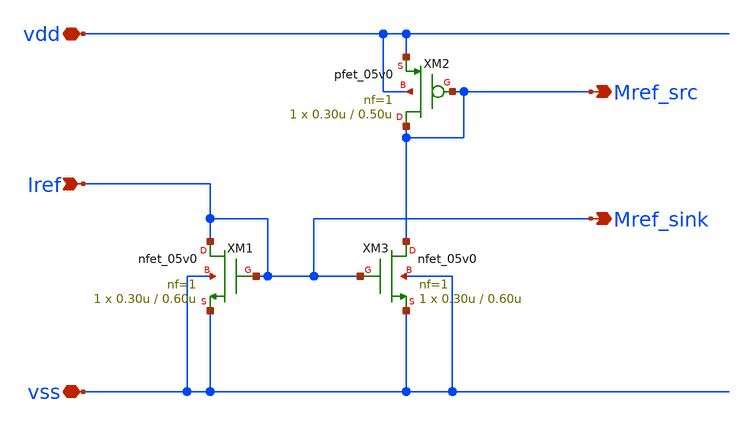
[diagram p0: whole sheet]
** sch_path: designs/libs/core_analog/iref/iref.sch
**.subckt iref Iref vdd vss Mref_src Mref_sink
*.ipin Iref
*.iopin vdd
*.iopin vss
*.opin Mref_src
*.opin Mref_sink
XM2 Mref_src Mref_src vdd vdd pfet_05v0 L=0.50u W=0.30u nf=1 ad='int((nf+1)/2) * W/nf * 0.18u' as='int((nf+2)/2) * W/nf * 0.18u'
+ pd='2*int((nf+1)/2) * (W/nf + 0.18u)' ps='2*int((nf+2)/2) * (W/nf + 0.18u)' nrd='0.18u / W' nrs='0.18u / W'
+ sa=0 sb=0 sd=0 m=1
XM1 Iref Iref vss vss nfet_05v0 L=0.60u W=0.30u nf=1 ad='int((nf+1)/2) * W/nf * 0.18u' as='int((nf+2)/2) * W/nf * 0.18u'
+ pd='2*int((nf+1)/2) * (W/nf + 0.18u)' ps='2*int((nf+2)/2) * (W/nf + 0.18u)' nrd='0.18u / W' nrs='0.18u / W'
+ sa=0 sb=0 sd=0 m=1
XM3 Mref_src Iref vss vss nfet_05v0 L=0.60u W=0.30u nf=1 ad='int((nf+1)/2) * W/nf * 0.18u' as='int((nf+2)/2) * W/nf * 0.18u'
+ pd='2*int((nf+1)/2) * (W/nf + 0.18u)' ps='2*int((nf+2)/2) * (W/nf + 0.18u)' nrd='0.18u / W' nrs='0.18u / W'
+ sa=0 sb=0 sd=0 m=1
**.ends
.end
